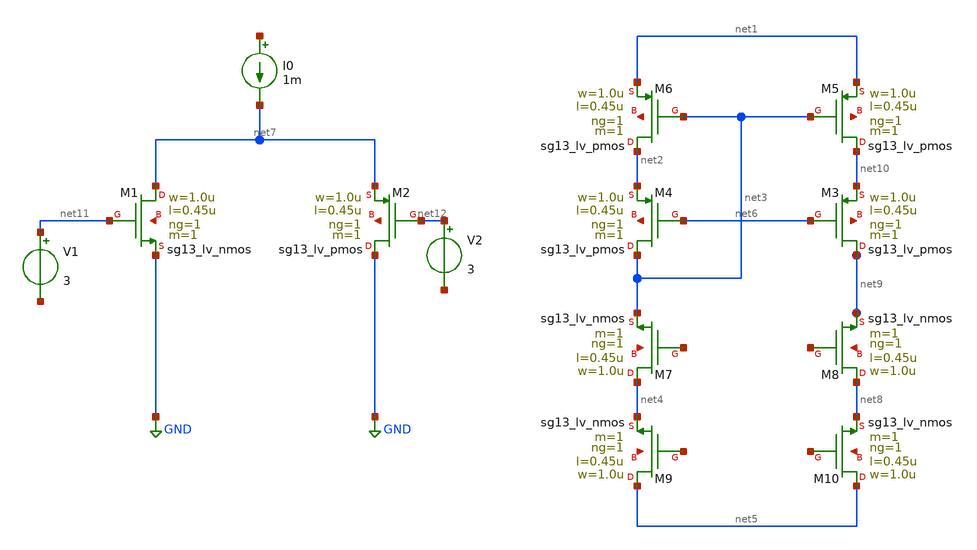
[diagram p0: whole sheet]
** sch_path: exp/IHP130/UnittyGain/sch/unitty_gain.sch
**.subckt unitty_gain
XM1 net7 net11 GND net13 sg13_lv_nmos w=1.0u l=0.45u ng=1 m=1 mm_ok=1
XM2 GND net12 net7 net14 sg13_lv_pmos w=1.0u l=0.45u ng=1 m=1 mm_ok=1
XM3 net9 net6 net10 net15 sg13_lv_pmos w=1.0u l=0.45u ng=1 m=1 mm_ok=1
XM4 net3 net6 net2 net16 sg13_lv_pmos w=1.0u l=0.45u ng=1 m=1 mm_ok=1
XM5 net10 net3 net1 net17 sg13_lv_pmos w=1.0u l=0.45u ng=1 m=1 mm_ok=1
XM6 net2 net3 net1 net18 sg13_lv_pmos w=1.0u l=0.45u ng=1 m=1 mm_ok=1
XM7 net4 net19 net3 net20 sg13_lv_nmos w=1.0u l=0.45u ng=1 m=1 mm_ok=1
XM8 net8 net21 net9 net22 sg13_lv_nmos w=1.0u l=0.45u ng=1 m=1 mm_ok=1
XM9 net5 net23 net4 net24 sg13_lv_nmos w=1.0u l=0.45u ng=1 m=1 mm_ok=1
XM10 net5 net25 net8 net26 sg13_lv_nmos w=1.0u l=0.45u ng=1 m=1 mm_ok=1
V1 net11 net27 3
V2 net12 net28 3
I0 net29 net7 1m
**.ends
.GLOBAL GND
.end
